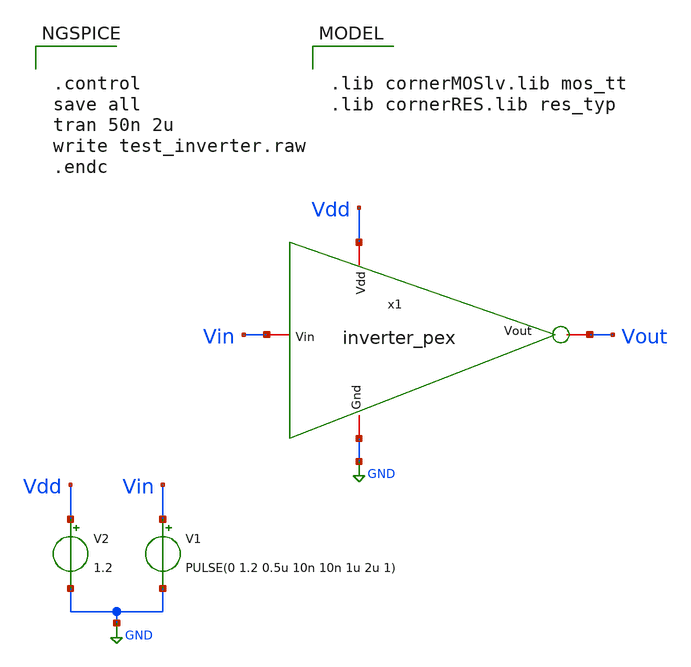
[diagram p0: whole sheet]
** sch_path: modules/module_3_8_bit_SAR_ADC/part_5_layout/components/inverter_example/pex/xschem/inverter_tb_pex.sch
**.subckt inverter_tb_pex
V1 Vin GND PULSE(0 1.2 0.5u 10n 10n 1u 2u 1)
V2 Vdd GND 1.2
x1 Vdd Vin Vout GND inverter_pex
**** begin user architecture code


.control
save all
tran 50n 2u
write test_inverter.raw
.endc



.lib cornerMOSlv.lib mos_tt
.lib cornerRES.lib res_typ


**** end user architecture code
**.ends

* expanding   symbol:  inverter_pex.sym # of pins=4
** sym_path: modules/module_0_foundations/inverter/inverter.sym

.subckt inverter_pex Vdd Vin Vout Gnd
X0 Vout Vin Vdd Vdd sg13_lv_pmos ad=0.68p pd=4.68u as=0.68p ps=4.68u w=2u l=0.45u
X1 Vout Vin Gnd Gnd sg13_lv_nmos ad=0.34p pd=2.68u as=0.34p ps=2.68u w=1u l=0.45u
C0 Vdd Vin 0.14482f
C1 Vout Vdd 0.13155f
C2 Vout Vin 0.10077f
R0 Vin Vin.n0 7.52248
C3 Vout Gnd 0.39245f
C4 Vin Gnd 0.64666f
C5 Vdd Gnd 0.15308f
.ends

.GLOBAL GND
.end
